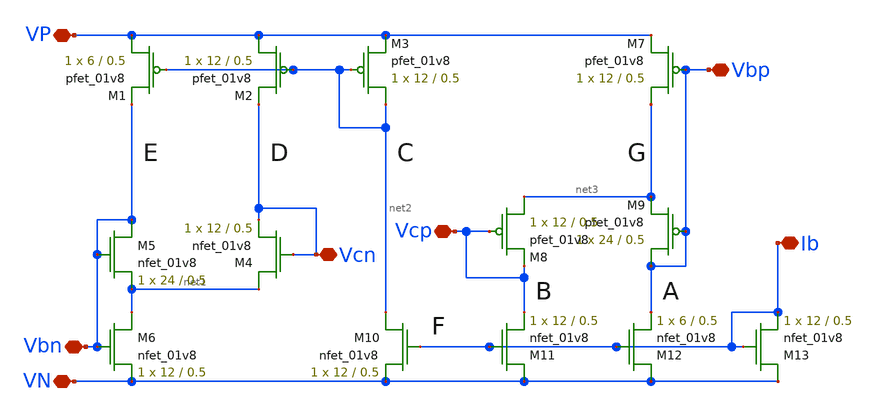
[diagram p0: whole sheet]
** sch_path: biascircuit1.sch
**.subckt biascircuit1 VP Ib VN Vcp Vbp Vbn Vcn
*.iopin VP
*.iopin Ib
*.iopin VN
*.iopin Vcp
*.iopin Vbp
*.iopin Vbn
*.iopin Vcn
XM5 Vbn Vbn net1 GND sky130_fd_pr__nfet_01v8 L=0.5 W=24 nf=1 ad='int((nf+1)/2) * W/nf * 0.29' as='int((nf+2)/2) * W/nf * 0.29'
+ pd='2*int((nf+1)/2) * (W/nf + 0.29)' ps='2*int((nf+2)/2) * (W/nf + 0.29)' nrd='0.29 / W' nrs='0.29 / W'
+ sa=0 sb=0 sd=0 mult=1 m=1
XM6 net1 Vbn VN GND sky130_fd_pr__nfet_01v8 L=0.5 W=12 nf=1 ad='int((nf+1)/2) * W/nf * 0.29' as='int((nf+2)/2) * W/nf * 0.29'
+ pd='2*int((nf+1)/2) * (W/nf + 0.29)' ps='2*int((nf+2)/2) * (W/nf + 0.29)' nrd='0.29 / W' nrs='0.29 / W'
+ sa=0 sb=0 sd=0 mult=1 m=1
XM4 net1 Vcn Vcn GND sky130_fd_pr__nfet_01v8 L=0.5 W=12 nf=1 ad='int((nf+1)/2) * W/nf * 0.29' as='int((nf+2)/2) * W/nf * 0.29'
+ pd='2*int((nf+1)/2) * (W/nf + 0.29)' ps='2*int((nf+2)/2) * (W/nf + 0.29)' nrd='0.29 / W' nrs='0.29 / W'
+ sa=0 sb=0 sd=0 mult=1 m=1
XM1 VP net2 Vbn VDD sky130_fd_pr__pfet_01v8 L=0.5 W=6 nf=1 ad='int((nf+1)/2) * W/nf * 0.29' as='int((nf+2)/2) * W/nf * 0.29'
+ pd='2*int((nf+1)/2) * (W/nf + 0.29)' ps='2*int((nf+2)/2) * (W/nf + 0.29)' nrd='0.29 / W' nrs='0.29 / W'
+ sa=0 sb=0 sd=0 mult=1 m=1
XM2 VP net2 Vcn VDD sky130_fd_pr__pfet_01v8 L=0.5 W=12 nf=1 ad='int((nf+1)/2) * W/nf * 0.29' as='int((nf+2)/2) * W/nf * 0.29'
+ pd='2*int((nf+1)/2) * (W/nf + 0.29)' ps='2*int((nf+2)/2) * (W/nf + 0.29)' nrd='0.29 / W' nrs='0.29 / W'
+ sa=0 sb=0 sd=0 mult=1 m=1
XM3 net2 net2 VP VDD sky130_fd_pr__pfet_01v8 L=0.5 W=12 nf=1 ad='int((nf+1)/2) * W/nf * 0.29' as='int((nf+2)/2) * W/nf * 0.29'
+ pd='2*int((nf+1)/2) * (W/nf + 0.29)' ps='2*int((nf+2)/2) * (W/nf + 0.29)' nrd='0.29 / W' nrs='0.29 / W'
+ sa=0 sb=0 sd=0 mult=1 m=1
XM9 Vbp Vbp net3 VDD sky130_fd_pr__pfet_01v8 L=0.5 W=24 nf=1 ad='int((nf+1)/2) * W/nf * 0.29' as='int((nf+2)/2) * W/nf * 0.29'
+ pd='2*int((nf+1)/2) * (W/nf + 0.29)' ps='2*int((nf+2)/2) * (W/nf + 0.29)' nrd='0.29 / W' nrs='0.29 / W'
+ sa=0 sb=0 sd=0 mult=1 m=1
XM11 VN Ib Vcp GND sky130_fd_pr__nfet_01v8 L=0.5 W=12 nf=1 ad='int((nf+1)/2) * W/nf * 0.29' as='int((nf+2)/2) * W/nf * 0.29'
+ pd='2*int((nf+1)/2) * (W/nf + 0.29)' ps='2*int((nf+2)/2) * (W/nf + 0.29)' nrd='0.29 / W' nrs='0.29 / W'
+ sa=0 sb=0 sd=0 mult=1 m=1
XM10 net2 Ib VN GND sky130_fd_pr__nfet_01v8 L=0.5 W=12 nf=1 ad='int((nf+1)/2) * W/nf * 0.29' as='int((nf+2)/2) * W/nf * 0.29'
+ pd='2*int((nf+1)/2) * (W/nf + 0.29)' ps='2*int((nf+2)/2) * (W/nf + 0.29)' nrd='0.29 / W' nrs='0.29 / W'
+ sa=0 sb=0 sd=0 mult=1 m=1
XM8 net3 Vcp Vcp VDD sky130_fd_pr__pfet_01v8 L=0.5 W=12 nf=1 ad='int((nf+1)/2) * W/nf * 0.29' as='int((nf+2)/2) * W/nf * 0.29'
+ pd='2*int((nf+1)/2) * (W/nf + 0.29)' ps='2*int((nf+2)/2) * (W/nf + 0.29)' nrd='0.29 / W' nrs='0.29 / W'
+ sa=0 sb=0 sd=0 mult=1 m=1
XM12 VN Ib Vbp GND sky130_fd_pr__nfet_01v8 L=0.5 W=6 nf=1 ad='int((nf+1)/2) * W/nf * 0.29' as='int((nf+2)/2) * W/nf * 0.29'
+ pd='2*int((nf+1)/2) * (W/nf + 0.29)' ps='2*int((nf+2)/2) * (W/nf + 0.29)' nrd='0.29 / W' nrs='0.29 / W'
+ sa=0 sb=0 sd=0 mult=1 m=1
XM13 VN Ib Ib GND sky130_fd_pr__nfet_01v8 L=0.5 W=12 nf=1 ad='int((nf+1)/2) * W/nf * 0.29' as='int((nf+2)/2) * W/nf * 0.29'
+ pd='2*int((nf+1)/2) * (W/nf + 0.29)' ps='2*int((nf+2)/2) * (W/nf + 0.29)' nrd='0.29 / W' nrs='0.29 / W'
+ sa=0 sb=0 sd=0 mult=1 m=1
XM7 net3 Vbp VP VDD sky130_fd_pr__pfet_01v8 L=0.5 W=12 nf=1 ad='int((nf+1)/2) * W/nf * 0.29' as='int((nf+2)/2) * W/nf * 0.29'
+ pd='2*int((nf+1)/2) * (W/nf + 0.29)' ps='2*int((nf+2)/2) * (W/nf + 0.29)' nrd='0.29 / W' nrs='0.29 / W'
+ sa=0 sb=0 sd=0 mult=1 m=1
**.ends
.end
